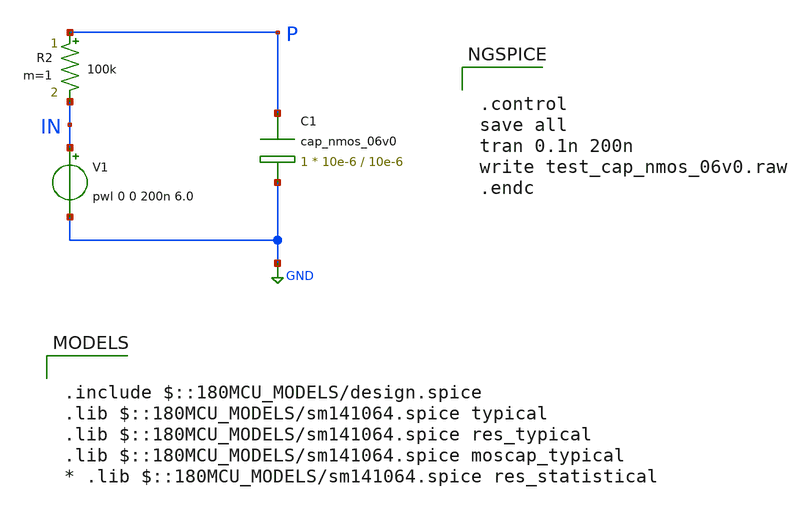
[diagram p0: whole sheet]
** sch_path: cells/xschem/tests/test_cap_nmos_06v0.sch
* Copyright 2022 GlobalFoundries PDK Authors
* Licensed under the Apache License, Version 2.0 (the "License");
* you may not use this file except in compliance with the License.
* You may obtain a copy of the License at
* https://www.apache.org/licenses/LICENSE-2.0
* Unless required by applicable law or agreed to in writing, software
* distributed under the License is distributed on an "AS IS" BASIS,
* WITHOUT WARRANTIES OR CONDITIONS OF ANY KIND, either express or implied.
* See the License for the specific language governing permissions and
* limitations under the License.
**.subckt test_cap_nmos_06v0
XC1 P GND cap_nmos_06v0 c_width=10e-6 c_length=10e-6 m=1
V1 IN GND pwl 0 0 200n 6.0
R2 P IN 100k m=1
**** begin user architecture code

.include $::180MCU_MODELS/design.spice
.lib $::180MCU_MODELS/sm141064.spice typical
.lib $::180MCU_MODELS/sm141064.spice res_typical
.lib $::180MCU_MODELS/sm141064.spice moscap_typical
* .lib $::180MCU_MODELS/sm141064.spice res_statistical



.control
save all
tran 0.1n 200n
write test_cap_nmos_06v0.raw
.endc


**** end user architecture code
**.ends
.GLOBAL GND
.end
